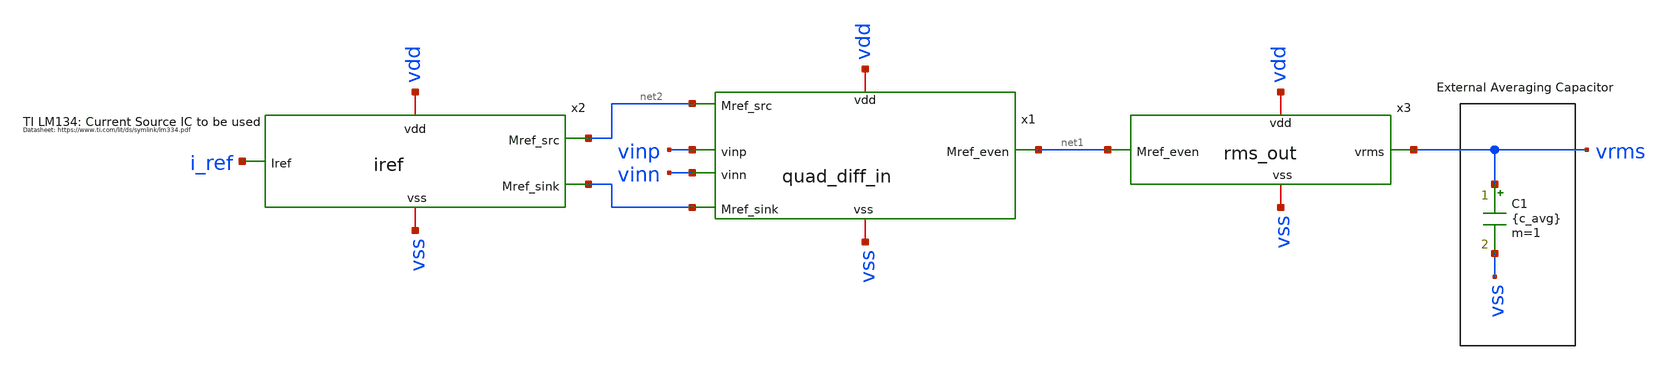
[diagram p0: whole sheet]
** sch_path: designs/libs/tb_analog/tb_rms_det/tb_rms_det.sch
**.subckt tb_rms_det
x1 vdd net2 net1 vinp vinn i_ref vss quad_diff_in
x2 vdd net2 i_ref vss iref
x3 vdd net1 vrms vss rms_out
C1 vrms vss {c_avg} m=1
**** begin user architecture code
External Averaging Capacitor
**** end user architecture code
**.ends

* expanding   symbol:  libs/core_analog/quad_diff_in/quad_diff_in.sym # of pins=7
** sym_path: libs/core_analog/quad_diff_in/quad_diff_in.sym
** sch_path: libs/core_analog/quad_diff_in/quad_diff_in.sch
.subckt quad_diff_in vdd Mref_src Mref_even vinp vinn Mref_sink vss
*.iopin vdd
*.iopin vss
*.ipin vinp
*.ipin vinn
*.ipin Mref_src
*.ipin Mref_sink
*.opin Mref_even
XM1 vdd vinp net1 vss nfet_05v0 L={L_UNIT} W={W_UNIT} nf=1 ad='int((nf+1)/2) * W/nf * 0.18u' as='int((nf+2)/2) * W/nf * 0.18u'
+ pd='2*int((nf+1)/2) * (W/nf + 0.18u)' ps='2*int((nf+2)/2) * (W/nf + 0.18u)' nrd='0.18u / W' nrs='0.18u / W'
+ sa=0 sb=0 sd=0 m={N_SKEW}
XM3 Mref_even vinp net2 vss nfet_05v0 L={L_UNIT} W={W_UNIT} nf=1 ad='int((nf+1)/2) * W/nf * 0.18u' as='int((nf+2)/2) * W/nf * 0.18u'
+ pd='2*int((nf+1)/2) * (W/nf + 0.18u)' ps='2*int((nf+2)/2) * (W/nf + 0.18u)' nrd='0.18u / W' nrs='0.18u / W'
+ sa=0 sb=0 sd=0 m=1
XM4 Mref_even vinn net1 vss nfet_05v0 L={L_UNIT} W={W_UNIT} nf=1 ad='int((nf+1)/2) * W/nf * 0.18u' as='int((nf+2)/2) * W/nf * 0.18u'
+ pd='2*int((nf+1)/2) * (W/nf + 0.18u)' ps='2*int((nf+2)/2) * (W/nf + 0.18u)' nrd='0.18u / W' nrs='0.18u / W'
+ sa=0 sb=0 sd=0 m=1
XM5 net1 Mref_sink vss vss nfet_05v0 L={L_BIAS} W={W_BIAS} nf=1 ad='int((nf+1)/2) * W/nf * 0.18u' as='int((nf+2)/2) * W/nf * 0.18u'
+ pd='2*int((nf+1)/2) * (W/nf + 0.18u)' ps='2*int((nf+2)/2) * (W/nf + 0.18u)' nrd='0.18u / W' nrs='0.18u / W'
+ sa=0 sb=0 sd=0 m={N_SKEW
XM6 net2 Mref_sink vss vss nfet_05v0 L={L_BIAS} W={W_BIAS} nf=1 ad='int((nf+1)/2) * W/nf * 0.18u' as='int((nf+2)/2)
+ * W/nf * 0.18u' pd='2*int((nf+1)/2) * (W/nf + 0.18u)' ps='2*int((nf+2)/2) * (W/nf + 0.18u)' nrd='0.18u
+ / W' nrs='0.18u / W' sa=0 sb=0 sd=0 m={N_SKEW
XM7 Mref_even Mref_src vdd vdd pfet_05v0 L={L_PBIAS} W={W_PBIAS} nf=1 ad='int((nf+1)/2) * W/nf * 0.18u'
+ as='int((nf+2)/2) * W/nf * 0.18u' pd='2*int((nf+1)/2) * (W/nf + 0.18u)' ps='2*int((nf+2)/2) * (W/nf + 0.18u)'
+ nrd='0.18u / W' nrs='0.18u / W' sa=0 sb=0 sd=0 m=1
XM8 Mref_even Mref_even vdd vdd pfet_05v0 L={L_EVEN} W={W_EVEN} nf=1 ad='int((nf+1)/2) * W/nf * 0.18u'
+ as='int((nf+2)/2) * W/nf * 0.18u' pd='2*int((nf+1)/2) * (W/nf + 0.18u)' ps='2*int((nf+2)/2) * (W/nf + 0.18u)'
+ nrd='0.18u / W' nrs='0.18u / W' sa=0 sb=0 sd=0 m=1
XM2 vdd vinn net2 vss nfet_05v0 L={L_UNIT} W={W_UNIT} nf=1 ad='int((nf+1)/2) * W/nf * 0.18u' as='int((nf+2)/2) * W/nf * 0.18u'
+ pd='2*int((nf+1)/2) * (W/nf + 0.18u)' ps='2*int((nf+2)/2) * (W/nf + 0.18u)' nrd='0.18u / W' nrs='0.18u / W'
+ sa=0 sb=0 sd=0 m={N_SKEW}
.ends


* expanding   symbol:  libs/core_analog/iref/iref.sym # of pins=5
** sym_path: designs/libs/core_analog/iref/iref.sym
** sch_path: designs/libs/core_analog/iref/iref.sch
.subckt iref vdd Mref_src Iref vss
*.ipin Iref
*.iopin vdd
*.iopin vss
*.opin Mref_src
*.opin Iref
XM2 Mref_src Mref_src vdd vdd pfet_05v0 L={L_PBIAS} W={W_PBIAS} nf=1 ad='int((nf+1)/2) * W/nf * 0.18u'
+ as='int((nf+2)/2) * W/nf * 0.18u' pd='2*int((nf+1)/2) * (W/nf + 0.18u)' ps='2*int((nf+2)/2) * (W/nf + 0.18u)'
+ nrd='0.18u / W' nrs='0.18u / W' sa=0 sb=0 sd=0 m=1
XM1 Iref Iref vss vss nfet_05v0 L={L_BIAS} W={W_BIAS} nf=1 ad='int((nf+1)/2) * W/nf * 0.18u' as='int((nf+2)/2) * W/nf * 0.18u'
+ pd='2*int((nf+1)/2) * (W/nf + 0.18u)' ps='2*int((nf+2)/2) * (W/nf + 0.18u)' nrd='0.18u / W' nrs='0.18u / W'
+ sa=0 sb=0 sd=0 m=1
XM3 Mref_src Iref vss vss nfet_05v0 L={L_BIAS} W={W_BIAS} nf=1 ad='int((nf+1)/2) * W/nf * 0.18u' as='int((nf+2)/2) * W/nf * 0.18u'
+ pd='2*int((nf+1)/2) * (W/nf + 0.18u)' ps='2*int((nf+2)/2) * (W/nf + 0.18u)' nrd='0.18u / W' nrs='0.18u / W'
+ sa=0 sb=0 sd=0 m=2
.ends


* expanding   symbol:  libs/core_analog/rms_out/rms_out.sym # of pins=4
** sym_path: libs/core_analog/rms_out/rms_out.sym
** sch_path: libs/core_analog/rms_out/rms_out.sch
.subckt rms_out vdd Mref_even vrms vss
*.ipin Mref_even
*.iopin vdd
*.iopin vss
*.opin vrms
XM1 vrms Mref_even vdd vdd pfet_05v0 L={L_EVEN} W={W_EVEN} nf=1 ad='int((nf+1)/2) * W/nf * 0.18u' as='int((nf+2)/2) * W/nf * 0.18u'
+ pd='2*int((nf+1)/2) * (W/nf + 0.18u)' ps='2*int((nf+2)/2) * (W/nf + 0.18u)' nrd='0.18u / W' nrs='0.18u / W'
+ sa=0 sb=0 sd=0 m={M_EVEN}
XM2 vrms vrms vss vss nfet_05v0 L={L_OUT} W={W_OUT} nf=1 ad='int((nf+1)/2) * W/nf * 0.18u' as='int((nf+2)/2) * W/nf * 0.18u'
+ pd='2*int((nf+1)/2) * (W/nf + 0.18u)' ps='2*int((nf+2)/2) * (W/nf + 0.18u)' nrd='0.18u / W' nrs='0.18u / W'
+ sa=0 sb=0 sd=0 m=1
.ends

.end
